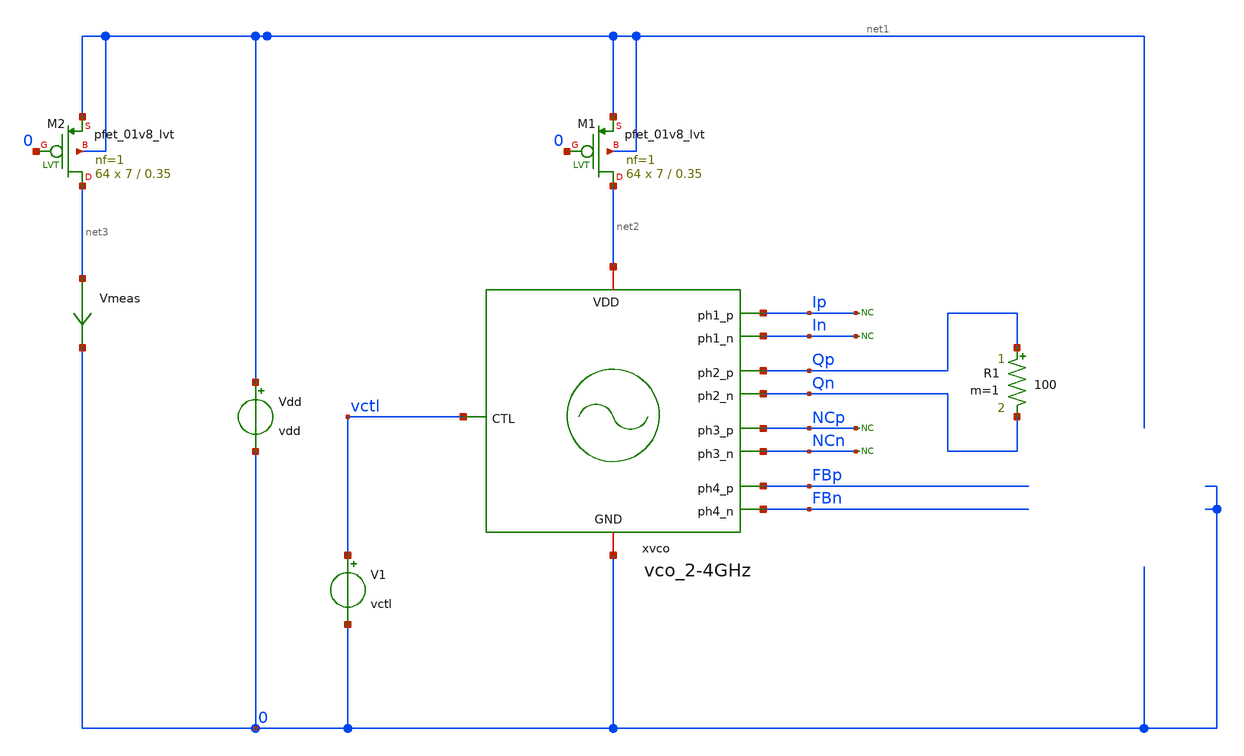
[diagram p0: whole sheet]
** sch_path: design/vco_2-4GHz/tests/vco_2-4GHz_tb.sch
**.subckt vco_2-4GHz_tb
V1 vctl 0 vctl
Vdd net1 0 vdd
xvco net2 Ip In Qp Qn NCp NCn FBp FBn vctl 0 vco_2-4GHz
* noconn Ip
* noconn In
* noconn NCp
* noconn NCn
XM1 net2 0 net1 net1 sky130_fd_pr__pfet_01v8_lvt L=0.35 W=7 nf=1 ad='W * 0.29' as='W * 0.29' pd='2 * (W + 0.29)'
+ ps='2 * (W + 0.29)' nrd='0.29 / W' nrs='0.29 / W' sa=0 sb=0 sd=0 mult=64 m=64
XM2 net3 0 net1 net1 sky130_fd_pr__pfet_01v8_lvt L=0.35 W=7 nf=1 ad='W * 0.29' as='W * 0.29' pd='2 * (W + 0.29)'
+ ps='2 * (W + 0.29)' nrd='0.29 / W' nrs='0.29 / W' sa=0 sb=0 sd=0 mult=64 m=64
Vmeas net3 0 0
.save i(vmeas)
R1 Qp Qn 100 m=1
**** begin user architecture code


.param temp=27
.temp 27

*.save v(ip) v(in) v(vctl) i(vdd)

.include sky130_fd_pr/cells/rf_nfet_01v8_lvt/sky130_fd_pr__rf_nfet_01v8_lvt_aM04W5p00L0p15.spice
.include sky130_fd_pr/cells/rf_nfet_01v8_lvt/sky130_fd_pr__rf_nfet_01v8_lvt_aM02W3p00L0p15.spice
.include sky130_fd_pr/cells/rf_nfet_01v8_lvt/sky130_fd_pr__rf_nfet_01v8_lvt_aM02W1p65L0p15.spice

.include sky130_fd_pr/cells/rf_pfet_01v8_lvt/sky130_fd_pr__rf_pfet_01v8_lvt_aM04W5p00L0p35.spice
.include sky130_fd_pr/cells/rf_pfet_01v8_lvt/sky130_fd_pr__rf_pfet_01v8_lvt_aM04W3p00L0p35.spice
.include sky130_fd_pr/cells/rf_pfet_01v8_lvt/sky130_fd_pr__rf_pfet_01v8_lvt_aM04W5p00L0p35.spice
.include sky130_fd_pr/cells/rf_pfet_01v8_lvt/sky130_fd_pr__rf_pfet_01v8_lvt_aM04W5p00L0p50.spice
.include sky130_fd_pr/cells/rf_pfet_01v8_lvt/sky130_fd_pr__rf_pfet_01v8_lvt_aM02W3p00L0p35.spice
.include sky130_fd_pr/cells/rf_pfet_01v8_lvt/sky130_fd_pr__rf_pfet_01v8_lvt_aM02W5p00L0p35.spice

.include sky130_fd_pr/cells/rf_pfet_01v8/sky130_fd_pr__rf_pfet_01v8_aM02W1p65L0p15.spice
.include sky130_fd_pr/cells/rf_pfet_01v8/sky130_fd_pr__rf_pfet_01v8_aM02W3p00L0p15.spice
.include sky130_fd_pr/cells/rf_pfet_01v8/sky130_fd_pr__rf_pfet_01v8_aM02W5p00L0p15.spice
.include sky130_fd_pr/cells/rf_pfet_01v8/sky130_fd_pr__rf_pfet_01v8_aM02W3p00L0p25.spice
.include sky130_fd_pr/cells/rf_pfet_01v8/sky130_fd_pr__rf_pfet_01v8_aM02W5p00L0p25.spice
.include sky130_fd_pr/cells/rf_pfet_01v8/sky130_fd_pr__rf_pfet_01v8_aF04W2p00L0p15.spice
.include sky130_fd_pr/cells/rf_pfet_01v8/sky130_fd_pr__rf_pfet_01v8_aF04W3p00L0p15.spice
.include sky130_fd_pr/cells/rf_pfet_01v8/sky130_fd_pr__rf_pfet_01v8_aM02W1p65L0p25.spice

.include sky130_fd_pr/cells/rf_nfet_01v8_lvt/sky130_fd_pr__rf_nfet_01v8_lvt_aF06W3p00L0p15.spice
.include sky130_fd_pr/cells/rf_nfet_01v8_lvt/sky130_fd_pr__rf_nfet_01v8_lvt_aF06W1p65L0p15.spice
.include sky130_fd_pr/cells/rf_nfet_01v8_lvt/sky130_fd_pr__rf_nfet_01v8_lvt_aF04W1p65L0p15.spice
.include sky130_fd_pr/cells/rf_nfet_01v8_lvt/sky130_fd_pr__rf_nfet_01v8_lvt_aF02W1p65L0p15.spice
.include sky130_fd_pr/cells/rf_nfet_01v8_lvt/sky130_fd_pr__rf_nfet_01v8_lvt_aF02W0p84L0p15.spice


.lib sky130_fd_pr/models/sky130.lib.spice tt
*.include sky130_fd_pr/models/corners/tt.spice


.tran 0.01n 10n uic
.param vdd=1.8
.param vctl=0.2


**** end user architecture code
**.ends
.end
